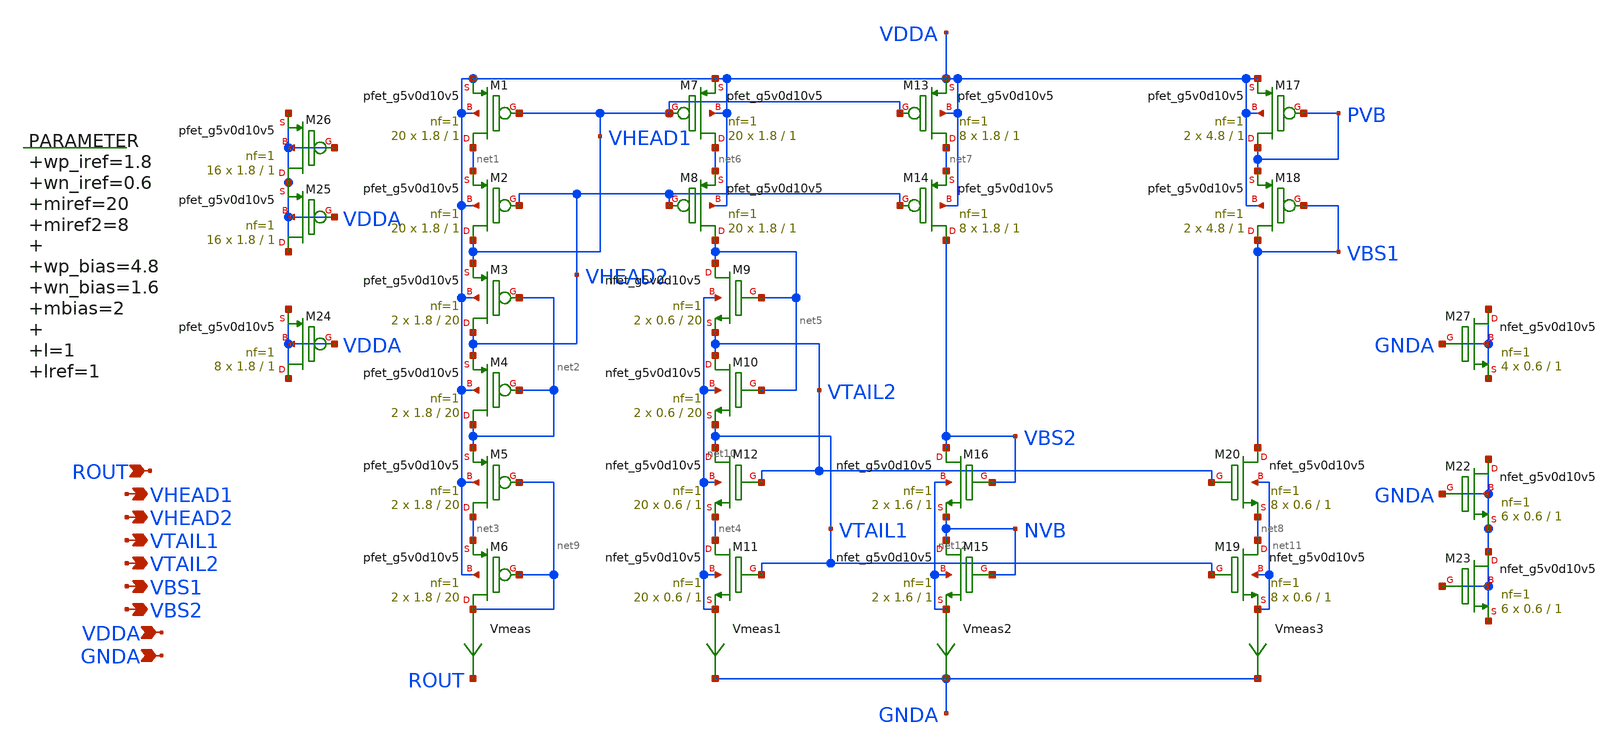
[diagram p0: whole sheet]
** sch_path: xschem/bias_opamp.sch
**.subckt bias_opamp ROUT VHEAD1 VDDA GNDA VHEAD2 VTAIL1 VTAIL2 VBS1 VBS2
*.ipin ROUT
*.opin VHEAD1
*.ipin VDDA
*.ipin GNDA
*.opin VHEAD2
*.opin VTAIL1
*.opin VTAIL2
*.opin VBS1
*.opin VBS2
.param wp_iref=1.8 wn_iref=0.6 miref=20 miref2=8 wp_bias=4.8 wn_bias=1.6 mbias=2 l=1 lref=1 lr=20
XM1 net1 VHEAD1 VDDA VDDA sky130_fd_pr__pfet_g5v0d10v5 L=1 W=1.8 nf=1 ad='int((nf+1)/2) * W/nf * 0.29'
+ as='int((nf+2)/2) * W/nf * 0.29' pd='2*int((nf+1)/2) * (W/nf + 0.29)' ps='2*int((nf+2)/2) * (W/nf + 0.29)'
+ nrd='0.29 / W' nrs='0.29 / W' sa=0 sb=0 sd=0 mult=20 m=20
XM2 VHEAD1 VHEAD2 net1 VDDA sky130_fd_pr__pfet_g5v0d10v5 L=1 W=1.8 nf=1 ad='int((nf+1)/2) * W/nf * 0.29'
+ as='int((nf+2)/2) * W/nf * 0.29' pd='2*int((nf+1)/2) * (W/nf + 0.29)' ps='2*int((nf+2)/2) * (W/nf + 0.29)'
+ nrd='0.29 / W' nrs='0.29 / W' sa=0 sb=0 sd=0 mult=20 m=20
XM7 net6 VHEAD1 VDDA VDDA sky130_fd_pr__pfet_g5v0d10v5 L=1 W=1.8 nf=1 ad='int((nf+1)/2) * W/nf * 0.29'
+ as='int((nf+2)/2) * W/nf * 0.29' pd='2*int((nf+1)/2) * (W/nf + 0.29)' ps='2*int((nf+2)/2) * (W/nf + 0.29)'
+ nrd='0.29 / W' nrs='0.29 / W' sa=0 sb=0 sd=0 mult=20 m=20
XM8 net5 VHEAD2 net6 VDDA sky130_fd_pr__pfet_g5v0d10v5 L=1 W=1.8 nf=1 ad='int((nf+1)/2) * W/nf * 0.29'
+ as='int((nf+2)/2) * W/nf * 0.29' pd='2*int((nf+1)/2) * (W/nf + 0.29)' ps='2*int((nf+2)/2) * (W/nf + 0.29)'
+ nrd='0.29 / W' nrs='0.29 / W' sa=0 sb=0 sd=0 mult=20 m=20
XM3 VHEAD2 net2 VHEAD1 VDDA sky130_fd_pr__pfet_g5v0d10v5 L=20 W=1.8 nf=1 ad='int((nf+1)/2) * W/nf * 0.29'
+ as='int((nf+2)/2) * W/nf * 0.29' pd='2*int((nf+1)/2) * (W/nf + 0.29)' ps='2*int((nf+2)/2) * (W/nf + 0.29)'
+ nrd='0.29 / W' nrs='0.29 / W' sa=0 sb=0 sd=0 mult=2 m=2
XM4 net2 net2 VHEAD2 VDDA sky130_fd_pr__pfet_g5v0d10v5 L=20 W=1.8 nf=1 ad='int((nf+1)/2) * W/nf * 0.29'
+ as='int((nf+2)/2) * W/nf * 0.29' pd='2*int((nf+1)/2) * (W/nf + 0.29)' ps='2*int((nf+2)/2) * (W/nf + 0.29)'
+ nrd='0.29 / W' nrs='0.29 / W' sa=0 sb=0 sd=0 mult=2 m=2
XM5 net3 net9 net2 VDDA sky130_fd_pr__pfet_g5v0d10v5 L=20 W=1.8 nf=1 ad='int((nf+1)/2) * W/nf * 0.29'
+ as='int((nf+2)/2) * W/nf * 0.29' pd='2*int((nf+1)/2) * (W/nf + 0.29)' ps='2*int((nf+2)/2) * (W/nf + 0.29)'
+ nrd='0.29 / W' nrs='0.29 / W' sa=0 sb=0 sd=0 mult=2 m=2
XM6 net9 net9 net3 VDDA sky130_fd_pr__pfet_g5v0d10v5 L=20 W=1.8 nf=1 ad='int((nf+1)/2) * W/nf * 0.29'
+ as='int((nf+2)/2) * W/nf * 0.29' pd='2*int((nf+1)/2) * (W/nf + 0.29)' ps='2*int((nf+2)/2) * (W/nf + 0.29)'
+ nrd='0.29 / W' nrs='0.29 / W' sa=0 sb=0 sd=0 mult=2 m=2
XM13 net7 VHEAD1 VDDA VDDA sky130_fd_pr__pfet_g5v0d10v5 L=1 W=1.8 nf=1 ad='int((nf+1)/2) * W/nf * 0.29'
+ as='int((nf+2)/2) * W/nf * 0.29' pd='2*int((nf+1)/2) * (W/nf + 0.29)' ps='2*int((nf+2)/2) * (W/nf + 0.29)'
+ nrd='0.29 / W' nrs='0.29 / W' sa=0 sb=0 sd=0 mult=8 m=8
XM14 VBS2 VHEAD2 net7 VDDA sky130_fd_pr__pfet_g5v0d10v5 L=1 W=1.8 nf=1 ad='int((nf+1)/2) * W/nf * 0.29'
+ as='int((nf+2)/2) * W/nf * 0.29' pd='2*int((nf+1)/2) * (W/nf + 0.29)' ps='2*int((nf+2)/2) * (W/nf + 0.29)'
+ nrd='0.29 / W' nrs='0.29 / W' sa=0 sb=0 sd=0 mult=8 m=8
XM17 PVB PVB VDDA VDDA sky130_fd_pr__pfet_g5v0d10v5 L=1 W=4.8 nf=1 ad='int((nf+1)/2) * W/nf * 0.29' as='int((nf+2)/2) * W/nf * 0.29'
+ pd='2*int((nf+1)/2) * (W/nf + 0.29)' ps='2*int((nf+2)/2) * (W/nf + 0.29)' nrd='0.29 / W' nrs='0.29 / W'
+ sa=0 sb=0 sd=0 mult=2 m=2
XM18 VBS1 VBS1 PVB VDDA sky130_fd_pr__pfet_g5v0d10v5 L=1 W=4.8 nf=1 ad='int((nf+1)/2) * W/nf * 0.29'
+ as='int((nf+2)/2) * W/nf * 0.29' pd='2*int((nf+1)/2) * (W/nf + 0.29)' ps='2*int((nf+2)/2) * (W/nf + 0.29)'
+ nrd='0.29 / W' nrs='0.29 / W' sa=0 sb=0 sd=0 mult=2 m=2
XM11 net4 VTAIL1 net10 net10 sky130_fd_pr__nfet_g5v0d10v5 L=1 W=0.6 nf=1 ad='int((nf+1)/2) * W/nf * 0.29'
+ as='int((nf+2)/2) * W/nf * 0.29' pd='2*int((nf+1)/2) * (W/nf + 0.29)' ps='2*int((nf+2)/2) * (W/nf + 0.29)'
+ nrd='0.29 / W' nrs='0.29 / W' sa=0 sb=0 sd=0 mult=20 m=20
XM12 VTAIL1 VTAIL2 net4 net10 sky130_fd_pr__nfet_g5v0d10v5 L=1 W=0.6 nf=1 ad='int((nf+1)/2) * W/nf * 0.29'
+ as='int((nf+2)/2) * W/nf * 0.29' pd='2*int((nf+1)/2) * (W/nf + 0.29)' ps='2*int((nf+2)/2) * (W/nf + 0.29)'
+ nrd='0.29 / W' nrs='0.29 / W' sa=0 sb=0 sd=0 mult=20 m=20
XM9 net5 net5 VTAIL2 net10 sky130_fd_pr__nfet_g5v0d10v5 L=20 W=0.6 nf=1 ad='int((nf+1)/2) * W/nf * 0.29'
+ as='int((nf+2)/2) * W/nf * 0.29' pd='2*int((nf+1)/2) * (W/nf + 0.29)' ps='2*int((nf+2)/2) * (W/nf + 0.29)'
+ nrd='0.29 / W' nrs='0.29 / W' sa=0 sb=0 sd=0 mult=2 m=2
XM10 VTAIL2 net5 VTAIL1 net10 sky130_fd_pr__nfet_g5v0d10v5 L=20 W=0.6 nf=1 ad='int((nf+1)/2) * W/nf * 0.29'
+ as='int((nf+2)/2) * W/nf * 0.29' pd='2*int((nf+1)/2) * (W/nf + 0.29)' ps='2*int((nf+2)/2) * (W/nf + 0.29)'
+ nrd='0.29 / W' nrs='0.29 / W' sa=0 sb=0 sd=0 mult=2 m=2
XM22 GNDA GNDA GNDA GNDA sky130_fd_pr__nfet_g5v0d10v5 L=1 W=0.6 nf=1 ad='int((nf+1)/2) * W/nf * 0.29'
+ as='int((nf+2)/2) * W/nf * 0.29' pd='2*int((nf+1)/2) * (W/nf + 0.29)' ps='2*int((nf+2)/2) * (W/nf + 0.29)'
+ nrd='0.29 / W' nrs='0.29 / W' sa=0 sb=0 sd=0 mult=6 m=6
XM19 net8 VTAIL1 net11 net11 sky130_fd_pr__nfet_g5v0d10v5 L=1 W=0.6 nf=1 ad='int((nf+1)/2) * W/nf * 0.29'
+ as='int((nf+2)/2) * W/nf * 0.29' pd='2*int((nf+1)/2) * (W/nf + 0.29)' ps='2*int((nf+2)/2) * (W/nf + 0.29)'
+ nrd='0.29 / W' nrs='0.29 / W' sa=0 sb=0 sd=0 mult=8 m=8
XM20 VBS1 VTAIL2 net8 net11 sky130_fd_pr__nfet_g5v0d10v5 L=1 W=0.6 nf=1 ad='int((nf+1)/2) * W/nf * 0.29'
+ as='int((nf+2)/2) * W/nf * 0.29' pd='2*int((nf+1)/2) * (W/nf + 0.29)' ps='2*int((nf+2)/2) * (W/nf + 0.29)'
+ nrd='0.29 / W' nrs='0.29 / W' sa=0 sb=0 sd=0 mult=8 m=8
XM15 NVB NVB net12 net12 sky130_fd_pr__nfet_g5v0d10v5 L=1 W=1.6 nf=1 ad='int((nf+1)/2) * W/nf * 0.29'
+ as='int((nf+2)/2) * W/nf * 0.29' pd='2*int((nf+1)/2) * (W/nf + 0.29)' ps='2*int((nf+2)/2) * (W/nf + 0.29)'
+ nrd='0.29 / W' nrs='0.29 / W' sa=0 sb=0 sd=0 mult=2 m=2
XM16 VBS2 VBS2 NVB net12 sky130_fd_pr__nfet_g5v0d10v5 L=1 W=1.6 nf=1 ad='int((nf+1)/2) * W/nf * 0.29'
+ as='int((nf+2)/2) * W/nf * 0.29' pd='2*int((nf+1)/2) * (W/nf + 0.29)' ps='2*int((nf+2)/2) * (W/nf + 0.29)'
+ nrd='0.29 / W' nrs='0.29 / W' sa=0 sb=0 sd=0 mult=2 m=2
XM23 GNDA GNDA GNDA GNDA sky130_fd_pr__nfet_g5v0d10v5 L=1 W=0.6 nf=1 ad='int((nf+1)/2) * W/nf * 0.29'
+ as='int((nf+2)/2) * W/nf * 0.29' pd='2*int((nf+1)/2) * (W/nf + 0.29)' ps='2*int((nf+2)/2) * (W/nf + 0.29)'
+ nrd='0.29 / W' nrs='0.29 / W' sa=0 sb=0 sd=0 mult=6 m=6
XM24 VDDA VDDA VDDA VDDA sky130_fd_pr__pfet_g5v0d10v5 L=1 W=1.8 nf=1 ad='int((nf+1)/2) * W/nf * 0.29'
+ as='int((nf+2)/2) * W/nf * 0.29' pd='2*int((nf+1)/2) * (W/nf + 0.29)' ps='2*int((nf+2)/2) * (W/nf + 0.29)'
+ nrd='0.29 / W' nrs='0.29 / W' sa=0 sb=0 sd=0 mult=8 m=8
XM25 VDDA VDDA VDDA VDDA sky130_fd_pr__pfet_g5v0d10v5 L=1 W=1.8 nf=1 ad='int((nf+1)/2) * W/nf * 0.29'
+ as='int((nf+2)/2) * W/nf * 0.29' pd='2*int((nf+1)/2) * (W/nf + 0.29)' ps='2*int((nf+2)/2) * (W/nf + 0.29)'
+ nrd='0.29 / W' nrs='0.29 / W' sa=0 sb=0 sd=0 mult=16 m=16
XM26 VDDA VDDA VDDA VDDA sky130_fd_pr__pfet_g5v0d10v5 L=1 W=1.8 nf=1 ad='int((nf+1)/2) * W/nf * 0.29'
+ as='int((nf+2)/2) * W/nf * 0.29' pd='2*int((nf+1)/2) * (W/nf + 0.29)' ps='2*int((nf+2)/2) * (W/nf + 0.29)'
+ nrd='0.29 / W' nrs='0.29 / W' sa=0 sb=0 sd=0 mult=16 m=16
XM27 GNDA GNDA GNDA GNDA sky130_fd_pr__nfet_g5v0d10v5 L=1 W=0.6 nf=1 ad='int((nf+1)/2) * W/nf * 0.29'
+ as='int((nf+2)/2) * W/nf * 0.29' pd='2*int((nf+1)/2) * (W/nf + 0.29)' ps='2*int((nf+2)/2) * (W/nf + 0.29)'
+ nrd='0.29 / W' nrs='0.29 / W' sa=0 sb=0 sd=0 mult=4 m=4
Vmeas net9 ROUT 0
.save i(vmeas)
Vmeas1 net10 GNDA 0
.save i(vmeas1)
Vmeas2 net12 GNDA 0
.save i(vmeas2)
Vmeas3 net11 GNDA 0
.save i(vmeas3)
**.ends
.end
